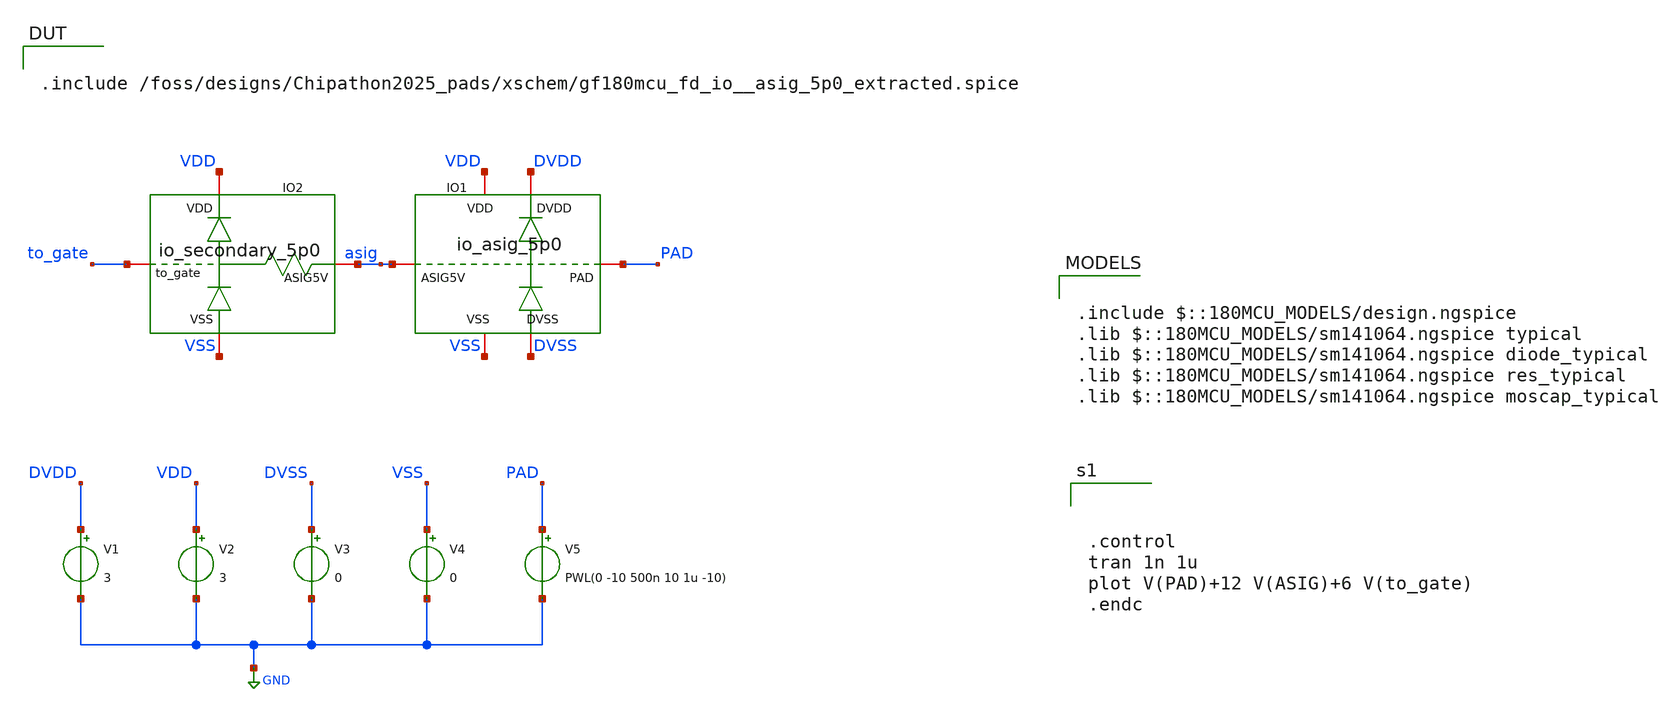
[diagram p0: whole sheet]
** sch_path: examples/pads_simulation/io_secondary_DC_tb.sch
**.subckt io_secondary_DC_tb
V1 DVDD GND 3
V2 VDD GND 3
V3 DVSS GND 0
V4 VSS GND 0
V5 PAD GND PWL(0 -10 500n 10 1u -10)
XIO1 DVSS DVDD VSS VDD PAD asig gf180mcu_fd_io__asig_5p0_extracted
XIO2 VDD to_gate asig VSS io_secondary_5p0
**** begin user architecture code

.include /foss/designs/Chipathon2025_pads/xschem/gf180mcu_fd_io__asig_5p0_extracted.spice


.include $::180MCU_MODELS/design.ngspice
.lib $::180MCU_MODELS/sm141064.ngspice typical
.lib $::180MCU_MODELS/sm141064.ngspice diode_typical
.lib $::180MCU_MODELS/sm141064.ngspice res_typical
.lib $::180MCU_MODELS/sm141064.ngspice moscap_typical




.control
tran 1n 1u
plot V(PAD)+12 V(ASIG)+6 V(to_gate)
.endc


**** end user architecture code
**.ends
.GLOBAL GND
.end
